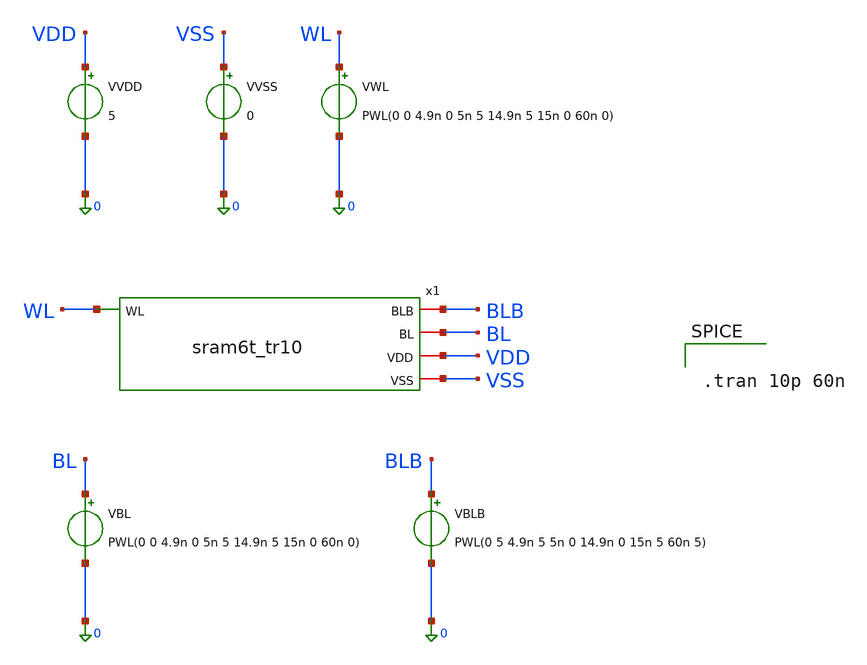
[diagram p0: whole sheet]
** sch_path: cell/tb_hold.sch
**.subckt tb_hold
VVDD VDD 0 5
VWL WL 0 PWL(0 0 4.9n 0 5n 5 14.9n 5 15n 0 60n 0)
VBL BL 0 PWL(0 0 4.9n 0 5n 5 14.9n 5 15n 0 60n 0)
VBLB BLB 0 PWL(0 5 4.9n 5 5n 0 14.9n 0 15n 5 60n 5)
VVSS VSS 0 0
x1 BL BLB WL VDD VSS sram6t_tr10
**** begin user architecture code
 .include $::LIB/ip62_models


.tran 10p 60n


**** end user architecture code
**.ends
.end
